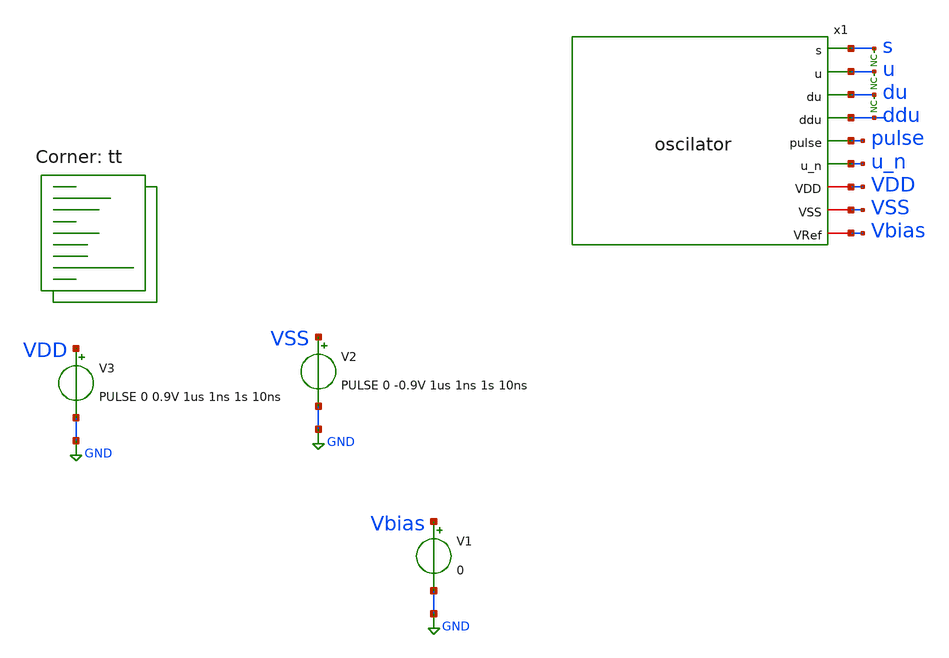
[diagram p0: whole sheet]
** sch_path: xschem/tests/oscilator/oscilator_test.sch
**.subckt oscilator_test
V3 VDD GND PULSE 0 0.9V 1us 1ns 1s 10ns
* noconn s
x1 s u du ddu pulse u_n VDD VSS Vbias oscilator
* noconn u
* noconn du
V1 Vbias GND 0
V2 VSS GND PULSE 0 -0.9V 1us 1ns 1s 10ns
**** begin user architecture code
 *.lib $::SKYWATER_MODELS/sky130.lib.spice tt
.include $::SKYWATER_STDCELLS/sky130_fd_sc_hd.spice



* Here's a comment
.options acct list
.options method=gear
.options maxord=1
.temp 25
*vvcc VDD 0 dc 1.8
*vvss VSS 0 0
.control
save all
ic v(u)=0.123
tran 0.01u 900u uic
plot u du s pulse u_n
plot u du s
* write oscilator_test.raw
wrdata oscillator_test2.csv u du s pulse
.endc


.lib $::SKYWATER_MODELS/sky130.lib.spice tt
**** end user architecture code
**.ends
.GLOBAL GND
.end
